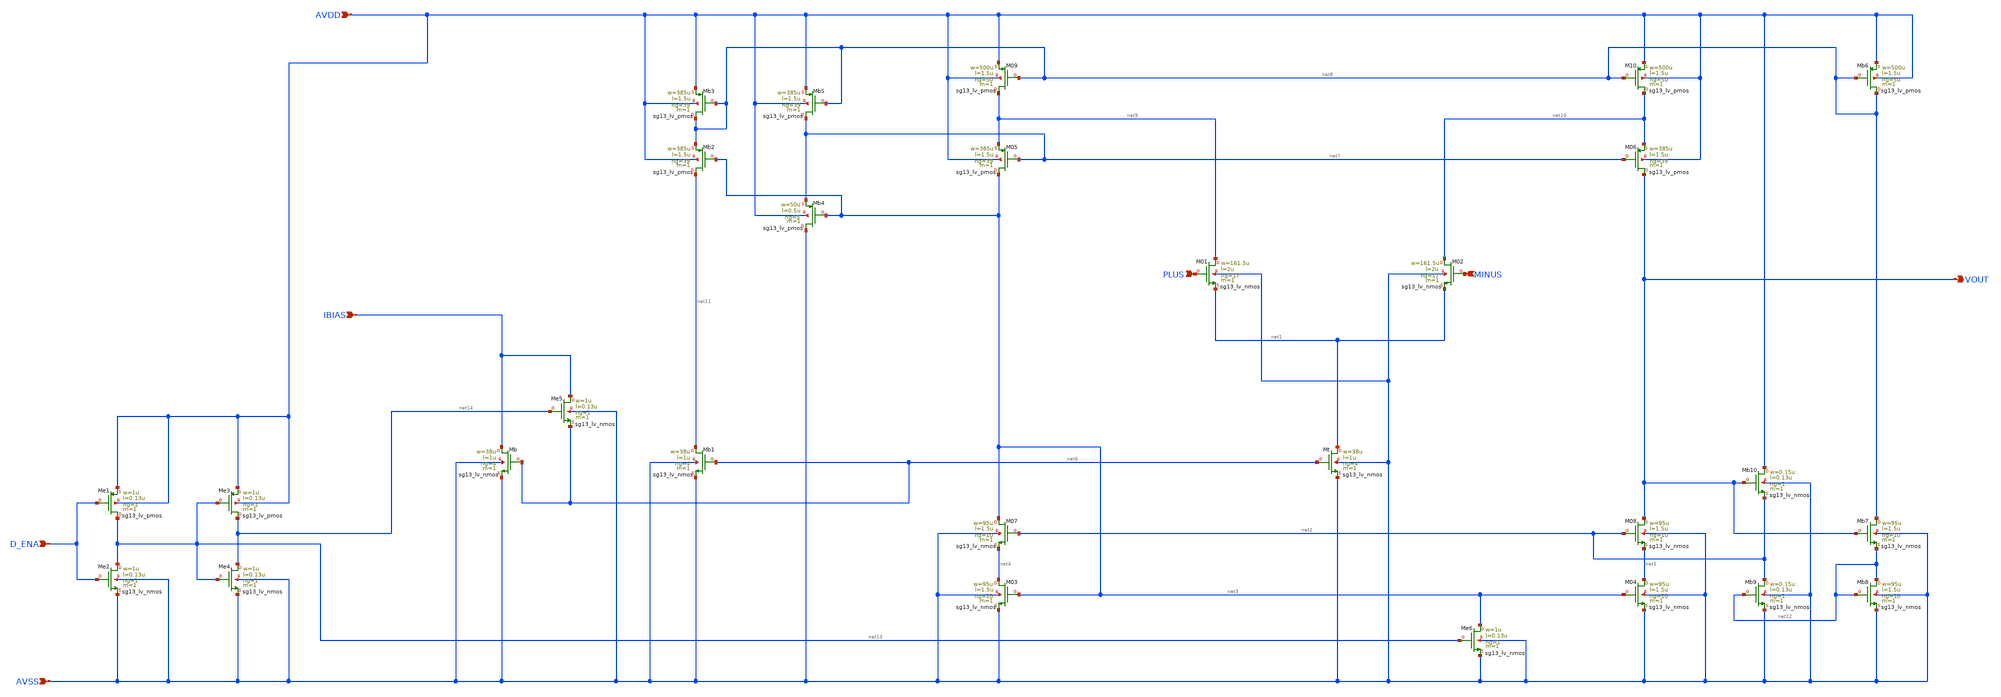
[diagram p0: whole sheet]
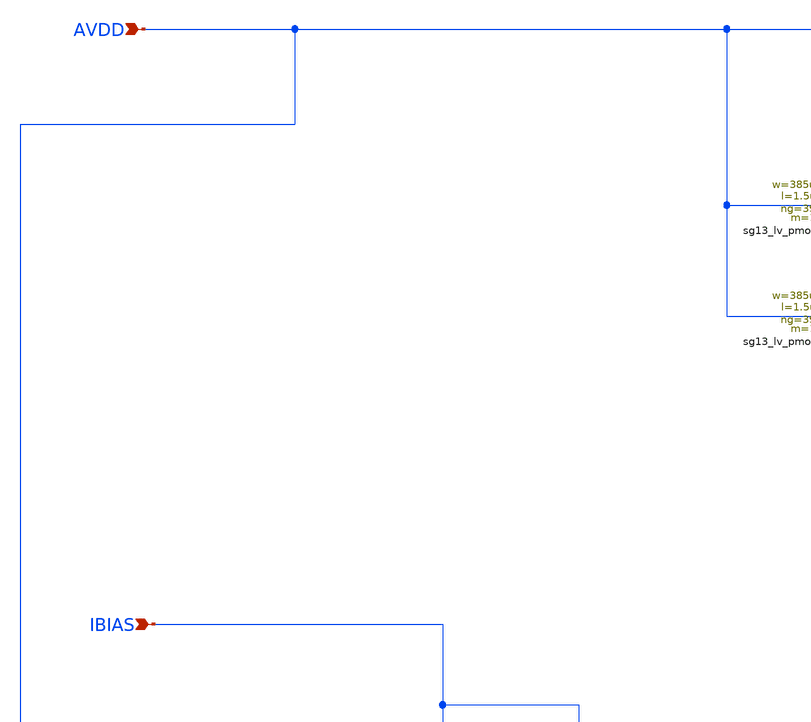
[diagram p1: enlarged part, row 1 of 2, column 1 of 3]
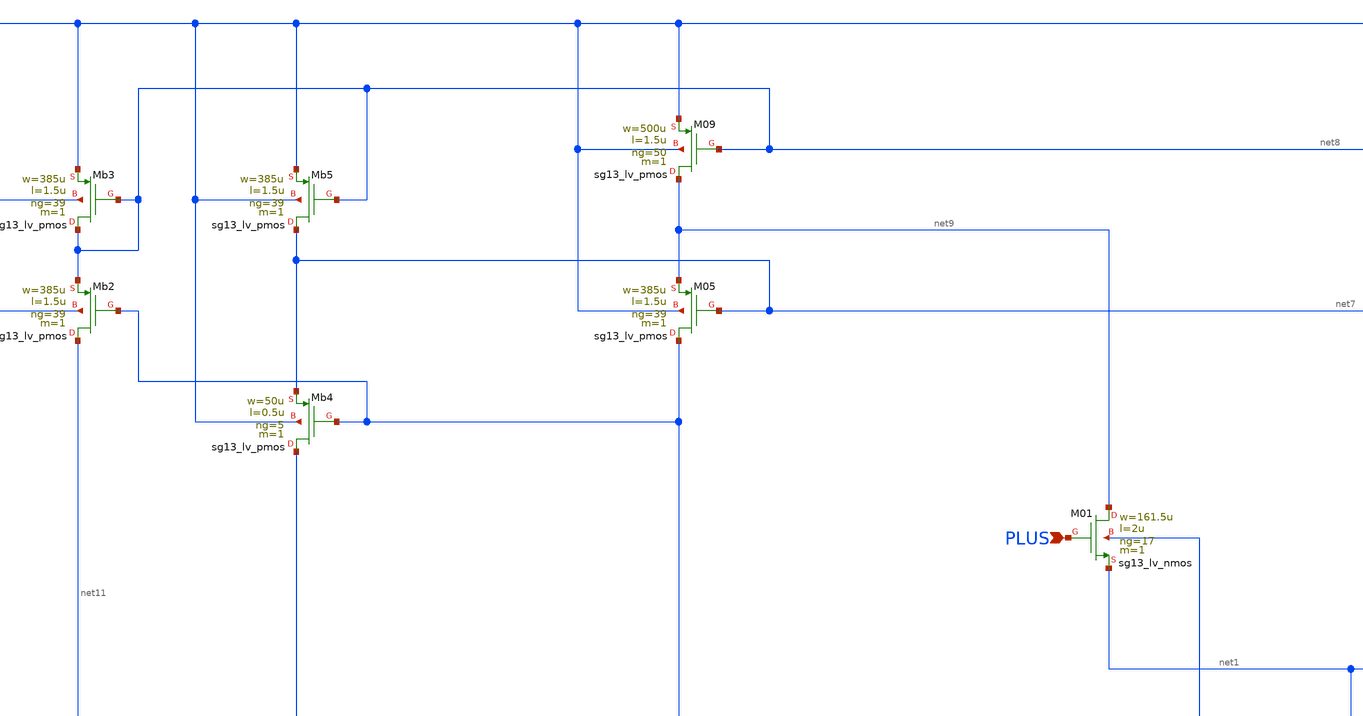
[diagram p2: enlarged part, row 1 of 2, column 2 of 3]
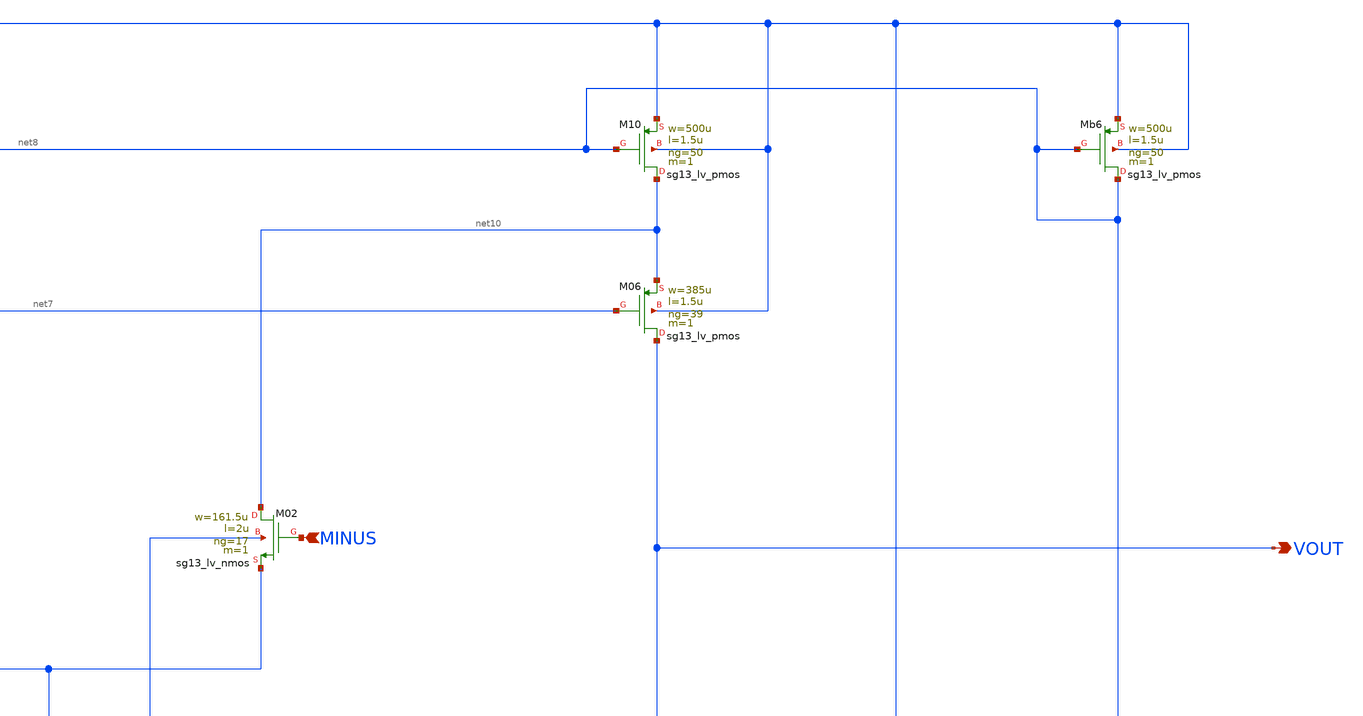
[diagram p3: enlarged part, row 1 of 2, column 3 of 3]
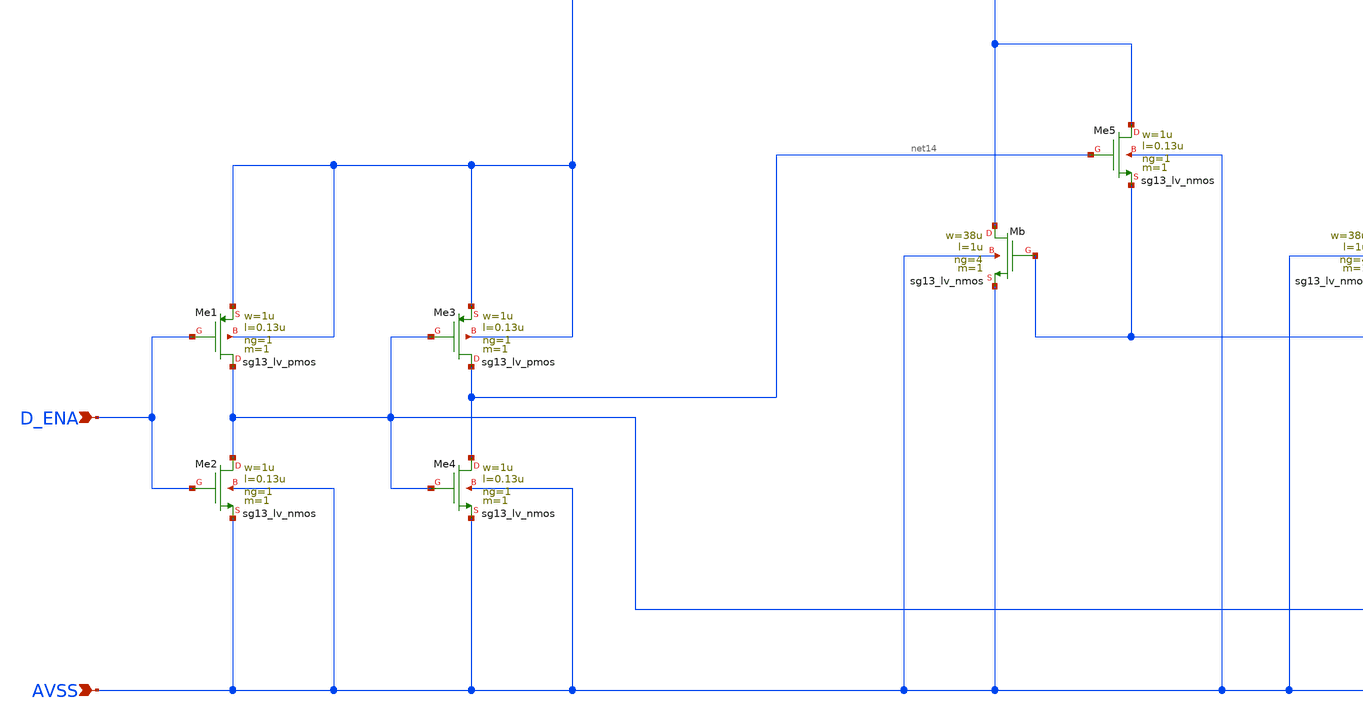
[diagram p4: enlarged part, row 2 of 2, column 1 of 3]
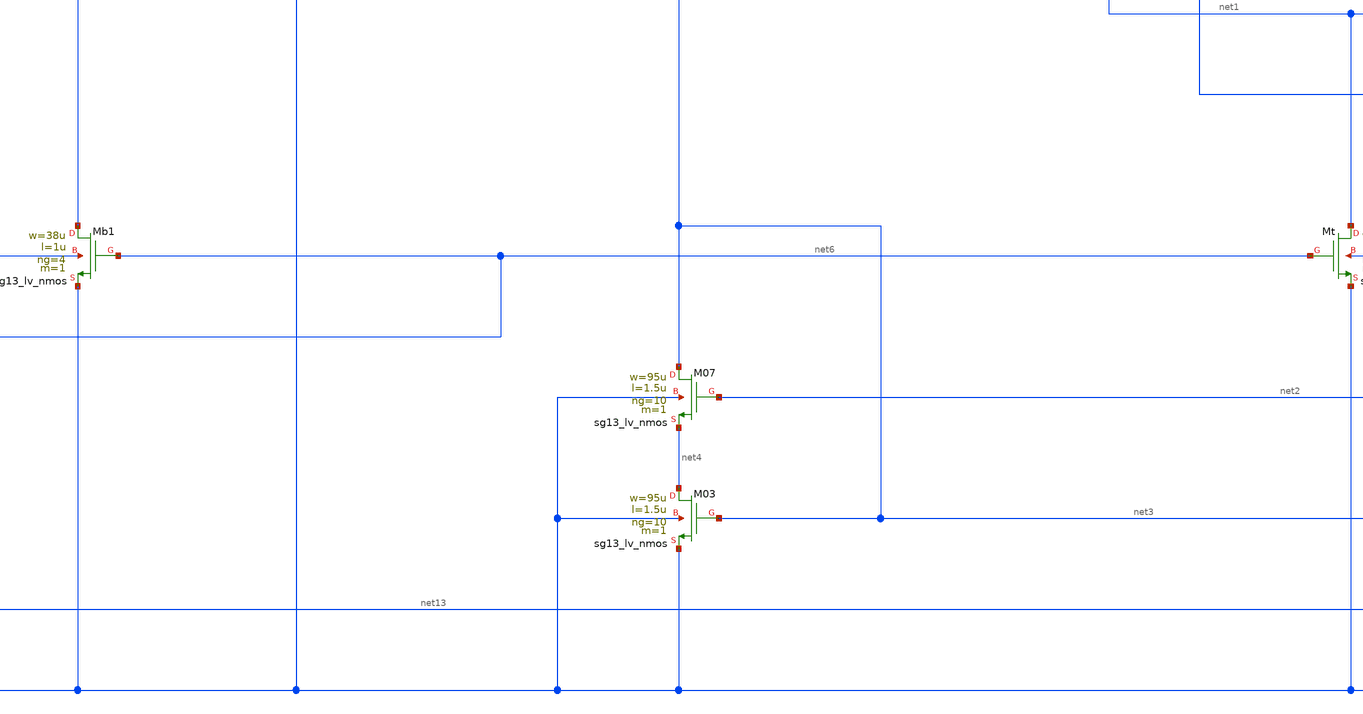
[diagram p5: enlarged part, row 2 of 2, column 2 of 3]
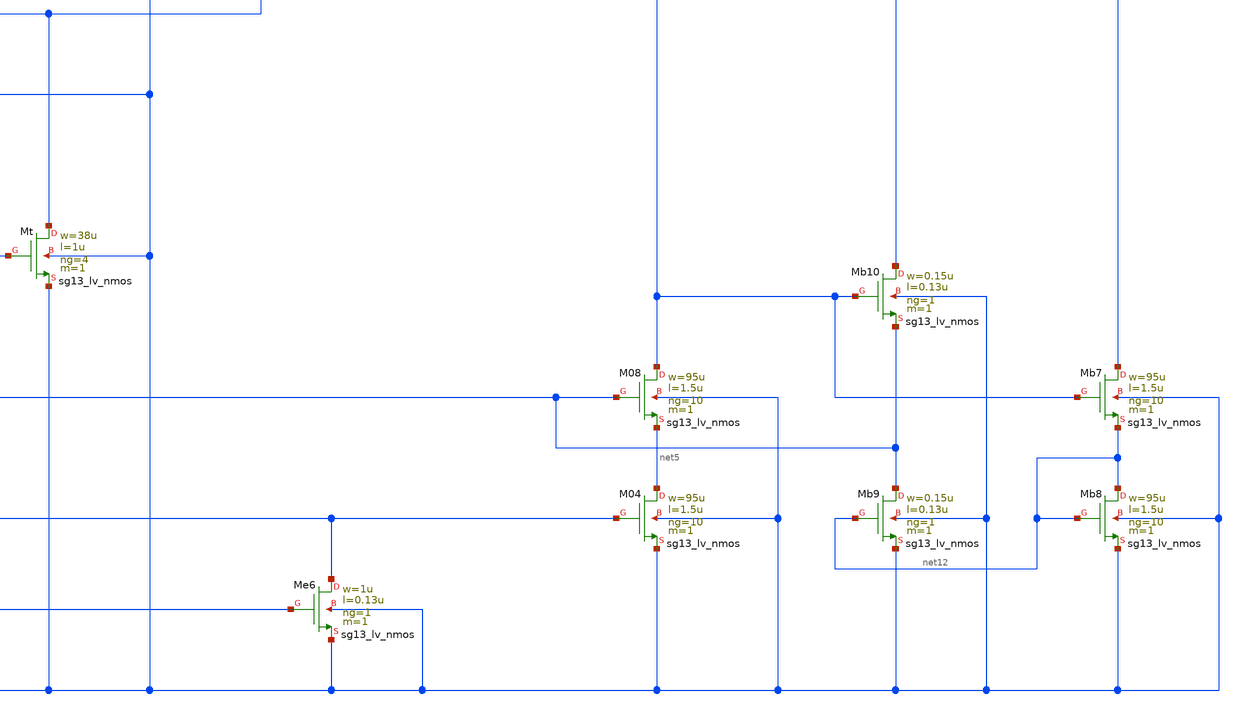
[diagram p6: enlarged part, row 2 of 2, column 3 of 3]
** sch_path: DSM_2ndOrder/1_Schematics/real_circuits/3v3/ota1_simple.sch
**.subckt ota1_simple VOUT MINUS PLUS AVSS IBIAS AVDD D_ENA
*.opin VOUT
*.ipin MINUS
*.ipin PLUS
*.ipin AVSS
*.ipin IBIAS
*.ipin AVDD
*.ipin D_ENA
XM01 net9 PLUS net1 AVSS sg13_lv_nmos w=161.5u l=2u ng=17 m=1 mm_ok=1
XM02 net10 MINUS net1 AVSS sg13_lv_nmos w=161.5u l=2u ng=17 m=1 mm_ok=1
XMt net1 net6 AVSS AVSS sg13_lv_nmos w=38u l=1u ng=4 m=1 mm_ok=1
XM08 VOUT net2 net5 AVSS sg13_lv_nmos w=95u l=1.5u ng=10 m=1 mm_ok=1
XM07 net3 net2 net4 AVSS sg13_lv_nmos w=95u l=1.5u ng=10 m=1 mm_ok=1
XM03 net4 net3 AVSS AVSS sg13_lv_nmos w=95u l=1.5u ng=10 m=1 mm_ok=1
XM04 net5 net3 AVSS AVSS sg13_lv_nmos w=95u l=1.5u ng=10 m=1 mm_ok=1
XMb1 net11 net6 AVSS AVSS sg13_lv_nmos w=38u l=1u ng=4 m=1 mm_ok=1
XM05 net3 net7 net9 AVDD sg13_lv_pmos w=385u l=1.5u ng=39 m=1 mm_ok=1
XM06 VOUT net7 net10 AVDD sg13_lv_pmos w=385u l=1.5u ng=39 m=1 mm_ok=1
XM09 net9 net8 AVDD AVDD sg13_lv_pmos w=500u l=1.5u ng=50 m=1 mm_ok=1
XM10 net10 net8 AVDD AVDD sg13_lv_pmos w=500u l=1.5u ng=50 m=1 mm_ok=1
XMb IBIAS net6 AVSS AVSS sg13_lv_nmos w=38u l=1u ng=4 m=1 mm_ok=1
XMb2 net11 net3 net8 AVDD sg13_lv_pmos w=385u l=1.5u ng=39 m=1 mm_ok=1
XMb3 net8 net8 AVDD AVDD sg13_lv_pmos w=385u l=1.5u ng=39 m=1 mm_ok=1
XMb5 net7 net8 AVDD AVDD sg13_lv_pmos w=385u l=1.5u ng=39 m=1 mm_ok=1
XMb4 AVSS net3 net7 AVDD sg13_lv_pmos w=50u l=0.5u ng=5 m=1 mm_ok=1
XMb10 AVDD VOUT net2 AVSS sg13_lv_nmos w=0.15u l=0.13u ng=1 m=1 mm_ok=1
XMb9 net2 net12 AVSS AVSS sg13_lv_nmos w=0.15u l=0.13u ng=1 m=1 mm_ok=1
XMb7 net8 VOUT net12 AVSS sg13_lv_nmos w=95u l=1.5u ng=10 m=1 mm_ok=1
XMb8 net12 net12 AVSS AVSS sg13_lv_nmos w=95u l=1.5u ng=10 m=1 mm_ok=1
XMb6 net8 net8 AVDD AVDD sg13_lv_pmos w=500u l=1.5u ng=50 m=1 mm_ok=1
XMe5 IBIAS net14 net6 AVSS sg13_lv_nmos w=1u l=0.13u ng=1 m=1 mm_ok=1
XMe2 net13 D_ENA AVSS AVSS sg13_lv_nmos w=1u l=0.13u ng=1 m=1 mm_ok=1
XMe4 net14 net13 AVSS AVSS sg13_lv_nmos w=1u l=0.13u ng=1 m=1 mm_ok=1
XMe6 net3 net13 AVSS AVSS sg13_lv_nmos w=1u l=0.13u ng=1 m=1 mm_ok=1
XMe3 net14 net13 AVDD AVDD sg13_lv_pmos w=1u l=0.13u ng=1 m=1 mm_ok=1
XMe1 net13 D_ENA AVDD AVDD sg13_lv_pmos w=1u l=0.13u ng=1 m=1 mm_ok=1
**.ends
.end
